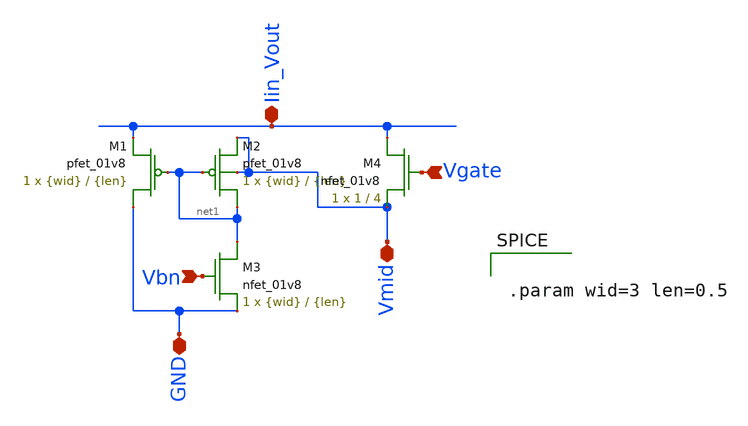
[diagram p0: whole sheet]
** sch_path: final/schematics/IV_converter.sch
**.subckt IV_converter Iin_Vout GND Vmid Vbn Vgate
*.iopin Iin_Vout
*.iopin GND
*.iopin Vmid
*.ipin Vbn
*.ipin Vgate
XM1 GND net1 Iin_Vout VDD sky130_fd_pr__pfet_01v8 L={len} W={wid} nf=1 ad='int((nf+1)/2) * W/nf * 0.29'
+ as='int((nf+2)/2) * W/nf * 0.29' pd='2*int((nf+1)/2) * (W/nf + 0.29)' ps='2*int((nf+2)/2) * (W/nf + 0.29)'
+ nrd='0.29 / W' nrs='0.29 / W' sa=0 sb=0 sd=0 mult=1 m=1
XM2 net1 net1 Vmid Vmid sky130_fd_pr__pfet_01v8 L={len} W={wid} nf=1 ad='int((nf+1)/2) * W/nf * 0.29'
+ as='int((nf+2)/2) * W/nf * 0.29' pd='2*int((nf+1)/2) * (W/nf + 0.29)' ps='2*int((nf+2)/2) * (W/nf + 0.29)'
+ nrd='0.29 / W' nrs='0.29 / W' sa=0 sb=0 sd=0 mult=1 m=1
XM3 net1 Vbn GND GND sky130_fd_pr__nfet_01v8 L={len} W={wid} nf=1 ad='int((nf+1)/2) * W/nf * 0.29' as='int((nf+2)/2) * W/nf * 0.29'
+ pd='2*int((nf+1)/2) * (W/nf + 0.29)' ps='2*int((nf+2)/2) * (W/nf + 0.29)' nrd='0.29 / W' nrs='0.29 / W'
+ sa=0 sb=0 sd=0 mult=1 m=1
XM4 Iin_Vout Vgate Vmid GND sky130_fd_pr__nfet_01v8 L=4 W=1 nf=1 ad='int((nf+1)/2) * W/nf * 0.29' as='int((nf+2)/2) * W/nf * 0.29'
+ pd='2*int((nf+1)/2) * (W/nf + 0.29)' ps='2*int((nf+2)/2) * (W/nf + 0.29)' nrd='0.29 / W' nrs='0.29 / W'
+ sa=0 sb=0 sd=0 mult=1 m=1
**** begin user architecture code


.param wid=3 len=0.5


**** end user architecture code
**.ends
.end
